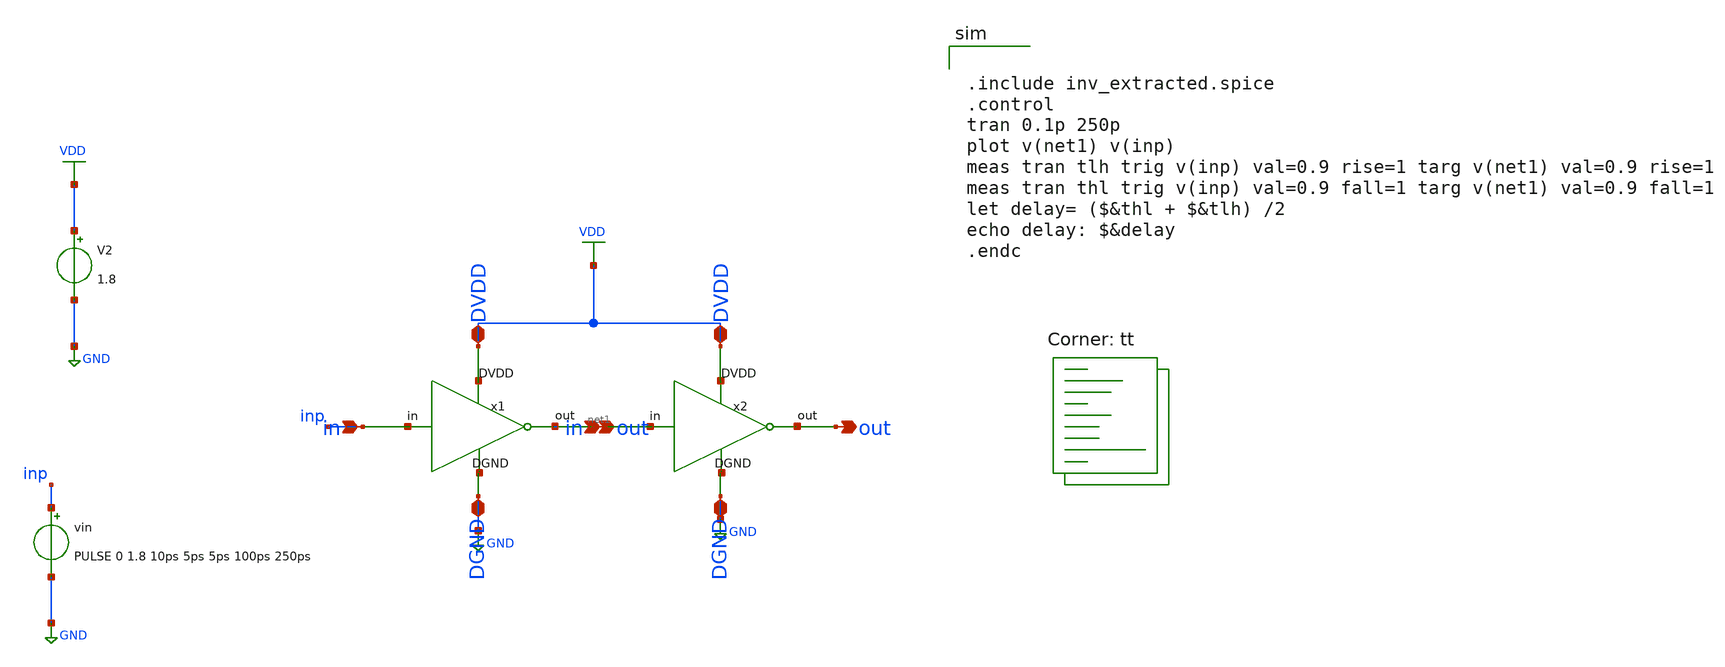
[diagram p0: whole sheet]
** sch_path: assignments/assignment4/tb1.sch
**.subckt tb1
x1 VDD inp net1 GND inv
x2 VDD net1 net2 GND inv
vin inp GND PULSE 0 1.8 10ps 5ps 5ps 100ps 250ps
V2 VDD GND 1.8
**** begin user architecture code


.include inv_extracted.spice
.control
tran 0.1p 250p
plot v(net1) v(inp)
meas tran tlh trig v(inp) val=0.9 rise=1 targ v(net1) val=0.9 rise=1
meas tran thl trig v(inp) val=0.9 fall=1 targ v(net1) val=0.9 fall=1
let delay= ($&thl + $&tlh) /2
echo delay: $&delay
.endc


.lib $::SKYWATER_MODELS/sky130.lib.spice tt
**** end user architecture code
**.ends

* expanding   symbol:  inv.sym # of pins=8
** sym_path: assignments/assignment4/inv.sym
** sch_path: assignments/assignment4/inv.sch
.subckt inv DVDD in out DGND
*.ipin in
*.opin out
*.iopin DVDD
*.iopin DGND
XM3 out in DVDD DVDD sky130_fd_pr__pfet_01v8 L=0.15 W=0.84 nf=1 ad='int((nf+1)/2) * W/nf * 0.29' as='int((nf+2)/2) * W/nf * 0.29'
+ pd='2*int((nf+1)/2) * (W/nf + 0.29)' ps='2*int((nf+2)/2) * (W/nf + 0.29)' nrd='0.29 / W' nrs='0.29 / W'
+ sa=0 sb=0 sd=0 mult=1 m=1
XM2 out in DGND DGND sky130_fd_pr__nfet_01v8 L=0.15 W=0.42 nf=1 ad='int((nf+1)/2) * W/nf * 0.29' as='int((nf+2)/2) * W/nf * 0.29'
+ pd='2*int((nf+1)/2) * (W/nf + 0.29)' ps='2*int((nf+2)/2) * (W/nf + 0.29)' nrd='0.29 / W' nrs='0.29 / W'
+ sa=0 sb=0 sd=0 mult=1 m=1
.ends

.GLOBAL GND
.GLOBAL VDD
.end
